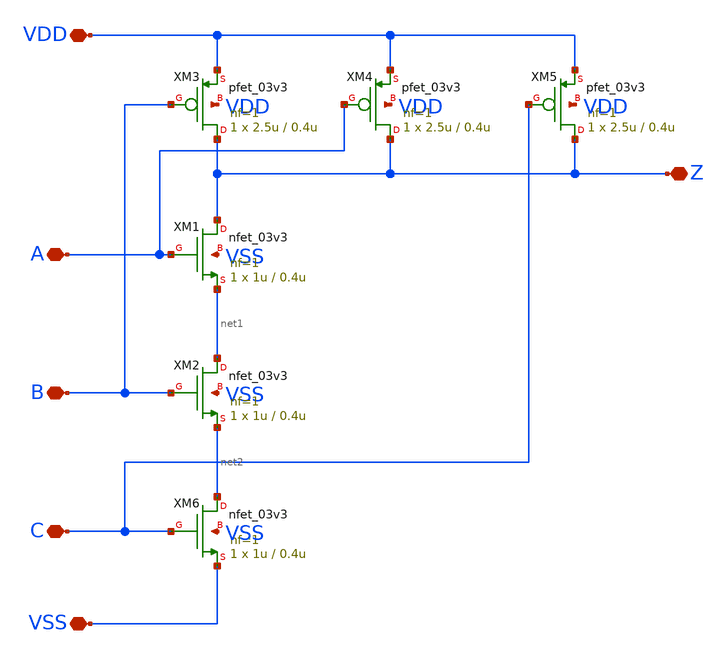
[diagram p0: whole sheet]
** sch_path: Analog/schematics/1_readout/slopedetector/dffrs/nand3.sch
**.subckt nand3 VDD VSS Z A B C
*.iopin VDD
*.iopin VSS
*.iopin Z
*.iopin A
*.iopin B
*.iopin C
XM1 Z A net1 VSS nfet_03v3 L=0.4u W=1u nf=1 ad='int((nf+1)/2) * W/nf * 0.18u' as='int((nf+2)/2) * W/nf * 0.18u'
+ pd='2*int((nf+1)/2) * (W/nf + 0.18u)' ps='2*int((nf+2)/2) * (W/nf + 0.18u)' nrd='0.18u / W' nrs='0.18u / W'
+ sa=0 sb=0 sd=0 m=1
XM2 net1 B net2 VSS nfet_03v3 L=0.4u W=1u nf=1 ad='int((nf+1)/2) * W/nf * 0.18u' as='int((nf+2)/2) * W/nf * 0.18u'
+ pd='2*int((nf+1)/2) * (W/nf + 0.18u)' ps='2*int((nf+2)/2) * (W/nf + 0.18u)' nrd='0.18u / W' nrs='0.18u / W'
+ sa=0 sb=0 sd=0 m=1
XM3 Z B VDD VDD pfet_03v3 L=0.4u W=2.5u nf=1 ad='int((nf+1)/2) * W/nf * 0.18u' as='int((nf+2)/2) * W/nf * 0.18u'
+ pd='2*int((nf+1)/2) * (W/nf + 0.18u)' ps='2*int((nf+2)/2) * (W/nf + 0.18u)' nrd='0.18u / W' nrs='0.18u / W'
+ sa=0 sb=0 sd=0 m=1
XM4 Z A VDD VDD pfet_03v3 L=0.4u W=2.5u nf=1 ad='int((nf+1)/2) * W/nf * 0.18u' as='int((nf+2)/2) * W/nf * 0.18u'
+ pd='2*int((nf+1)/2) * (W/nf + 0.18u)' ps='2*int((nf+2)/2) * (W/nf + 0.18u)' nrd='0.18u / W' nrs='0.18u / W'
+ sa=0 sb=0 sd=0 m=1
XM5 Z C VDD VDD pfet_03v3 L=0.4u W=2.5u nf=1 ad='int((nf+1)/2) * W/nf * 0.18u' as='int((nf+2)/2) * W/nf * 0.18u'
+ pd='2*int((nf+1)/2) * (W/nf + 0.18u)' ps='2*int((nf+2)/2) * (W/nf + 0.18u)' nrd='0.18u / W' nrs='0.18u / W'
+ sa=0 sb=0 sd=0 m=1
XM6 net2 C VSS VSS nfet_03v3 L=0.4u W=1u nf=1 ad='int((nf+1)/2) * W/nf * 0.18u' as='int((nf+2)/2) * W/nf * 0.18u'
+ pd='2*int((nf+1)/2) * (W/nf + 0.18u)' ps='2*int((nf+2)/2) * (W/nf + 0.18u)' nrd='0.18u / W' nrs='0.18u / W'
+ sa=0 sb=0 sd=0 m=1
**.ends
.end
